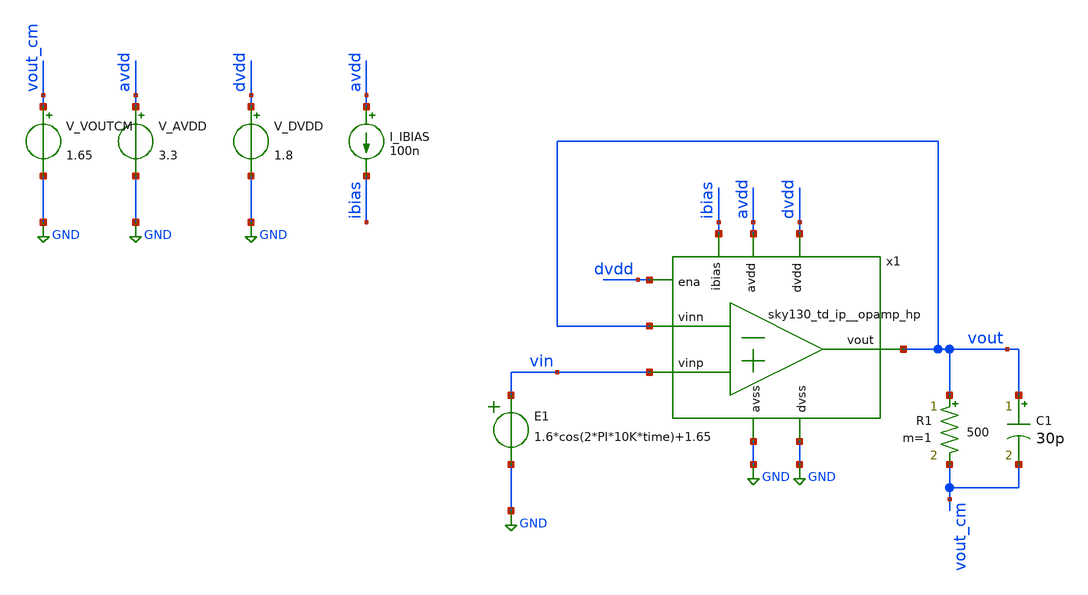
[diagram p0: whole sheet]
** sch_path: xschem/thd.sch
**.subckt thd
x1 avdd vout ibias vout vin GND dvdd GND dvdd sky130_td_ip__opamp_hp
V_AVDD avdd GND 3.3
.save i(v_avdd)
V_DVDD dvdd GND 1.8
.save i(v_dvdd)
I_IBIAS avdd ibias 100n
R1 vout vout_cm 500 m=1
C1 vout vout_cm 30p m=1
V_VOUTCM vout_cm GND 1.65
.save i(v_voutcm)
E1 vin GND VOL=' 1.6*cos(2*PI*10K*time)+1.65 '
**** begin user architecture code


.save all

.control
save all

tran 100n 1m
run

fourier 10e3 vout

* Try this:
* fourier 10e3 vout > somefile.dat

.endc




.lib /usr/local/share/pdk/sky130A/libs.tech/combined/sky130.lib.spice tt


**** end user architecture code
**.ends
.GLOBAL GND
.end
